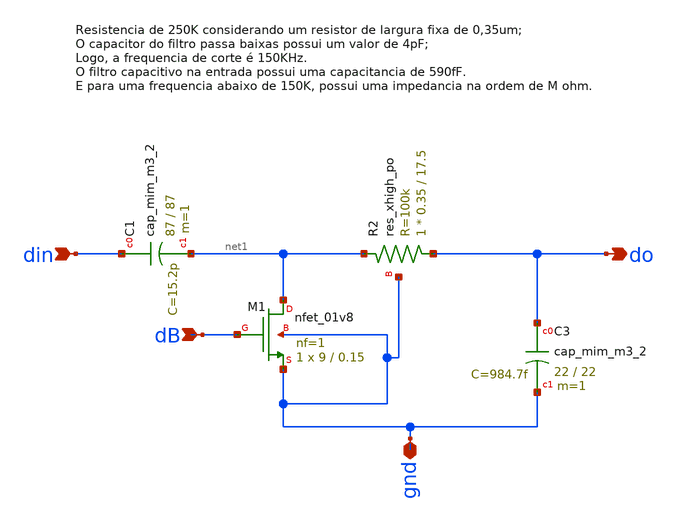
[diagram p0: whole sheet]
** sch_path: xschem/detectorPassivo.sch
**.subckt detectorPassivo din dB do gnd
*.ipin din
*.ipin dB
*.opin do
*.iopin gnd
XM1 net1 dB gnd gnd sky130_fd_pr__nfet_01v8 L=0.15 W=9 nf=1 ad='int((nf+1)/2) * W/nf * 0.29' as='int((nf+2)/2) * W/nf * 0.29'
+ pd='2*int((nf+1)/2) * (W/nf + 0.29)' ps='2*int((nf+2)/2) * (W/nf + 0.29)' nrd='0.29 / W' nrs='0.29 / W'
+ sa=0 sb=0 sd=0 mult=1 m=1
XC3 do gnd sky130_fd_pr__cap_mim_m3_2 W=22 L=22 MF=1 m=1
XR2 do net1 gnd sky130_fd_pr__res_xhigh_po W=0.35 L=17.5 mult=1 m=1
XC1 din net1 sky130_fd_pr__cap_mim_m3_2 W=87 L=87 MF=1 m=1
**.ends
.end
